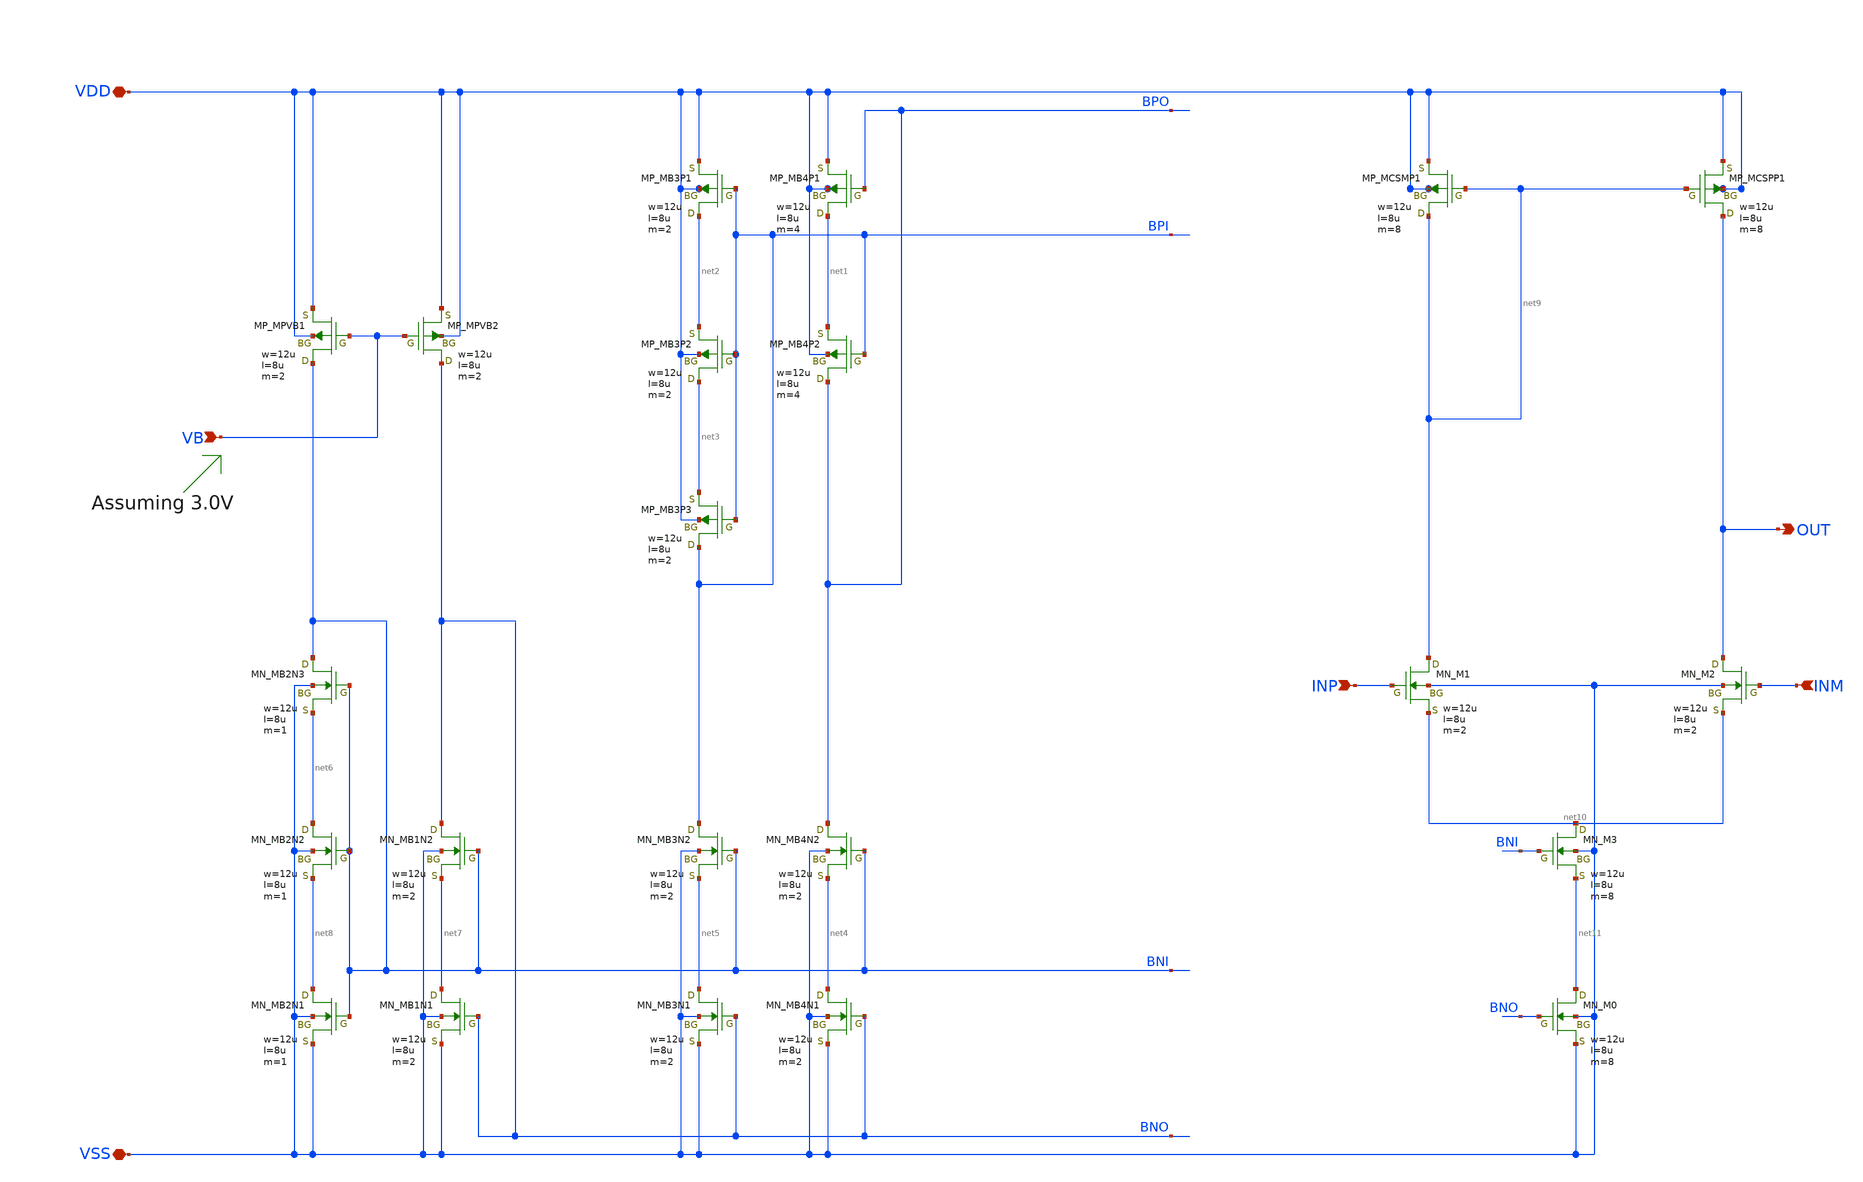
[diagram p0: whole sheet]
** sch_path: OpenSUSI-TR10/opamp_r2r/ota_ccm_1st.sch
**.subckt ota_ccm_1st VDD VSS INP INM VB OUT
*.iopin VDD
*.iopin VSS
*.ipin INP
*.ipin INM
*.ipin VB
*.opin OUT
XMB4P1 net1 BPO VDD VDD PMOS w=12u l=8u as=0 ad=0 ps=0 pd=0 nrd=0 nrs=0 m=4
XMB4P2 BPO BPI net1 VDD PMOS w=12u l=8u as=0 ad=0 ps=0 pd=0 nrd=0 nrs=0 m=4
XMB3P1 net2 BPI VDD VDD PMOS w=12u l=8u as=0 ad=0 ps=0 pd=0 nrd=0 nrs=0 m=2
XMB3P2 net3 BPI net2 VDD PMOS w=12u l=8u as=0 ad=0 ps=0 pd=0 nrd=0 nrs=0 m=2
XMB3P3 BPI BPI net3 VDD PMOS w=12u l=8u as=0 ad=0 ps=0 pd=0 nrd=0 nrs=0 m=2
XMB4N2 BPO BNI net4 VSS NMOS w=12u l=8u as=0 ad=0 ps=0 pd=0 nrd=0 nrs=0 m=2
XMB3N2 BPI BNI net5 VSS NMOS w=12u l=8u as=0 ad=0 ps=0 pd=0 nrd=0 nrs=0 m=2
XMB4N1 net4 BNO VSS VSS NMOS w=12u l=8u as=0 ad=0 ps=0 pd=0 nrd=0 nrs=0 m=2
XMB3N1 net5 BNO VSS VSS NMOS w=12u l=8u as=0 ad=0 ps=0 pd=0 nrd=0 nrs=0 m=2
XMB1N2 BNO BNI net7 VSS NMOS w=12u l=8u as=0 ad=0 ps=0 pd=0 nrd=0 nrs=0 m=2
XMB2N2 net6 BNI net8 VSS NMOS w=12u l=8u as=0 ad=0 ps=0 pd=0 nrd=0 nrs=0 m=1
XMB1N1 net7 BNO VSS VSS NMOS w=12u l=8u as=0 ad=0 ps=0 pd=0 nrd=0 nrs=0 m=2
XMB2N1 net8 BNI VSS VSS NMOS w=12u l=8u as=0 ad=0 ps=0 pd=0 nrd=0 nrs=0 m=1
XMB2N3 BNI BNI net6 VSS NMOS w=12u l=8u as=0 ad=0 ps=0 pd=0 nrd=0 nrs=0 m=1
XM3 net10 BNI net11 VSS NMOS w=12u l=8u as=0 ad=0 ps=0 pd=0 nrd=0 nrs=0 m=8
XM0 net11 BNO VSS VSS NMOS w=12u l=8u as=0 ad=0 ps=0 pd=0 nrd=0 nrs=0 m=8
XM1 net9 INP net10 VSS NMOS w=12u l=8u as=0 ad=0 ps=0 pd=0 nrd=0 nrs=0 m=2
XM2 OUT INM net10 VSS NMOS w=12u l=8u as=0 ad=0 ps=0 pd=0 nrd=0 nrs=0 m=2
XMCSMP1 net9 net9 VDD VDD PMOS w=12u l=8u as=0 ad=0 ps=0 pd=0 nrd=0 nrs=0 m=8
XMCSPP1 OUT net9 VDD VDD PMOS w=12u l=8u as=0 ad=0 ps=0 pd=0 nrd=0 nrs=0 m=8
XMPVB1 BNI VB VDD VDD PMOS w=12u l=8u as=0 ad=0 ps=0 pd=0 nrd=0 nrs=0 m=2
XMPVB2 BNO VB VDD VDD PMOS w=12u l=8u as=0 ad=0 ps=0 pd=0 nrd=0 nrs=0 m=2
**.ends
.end
